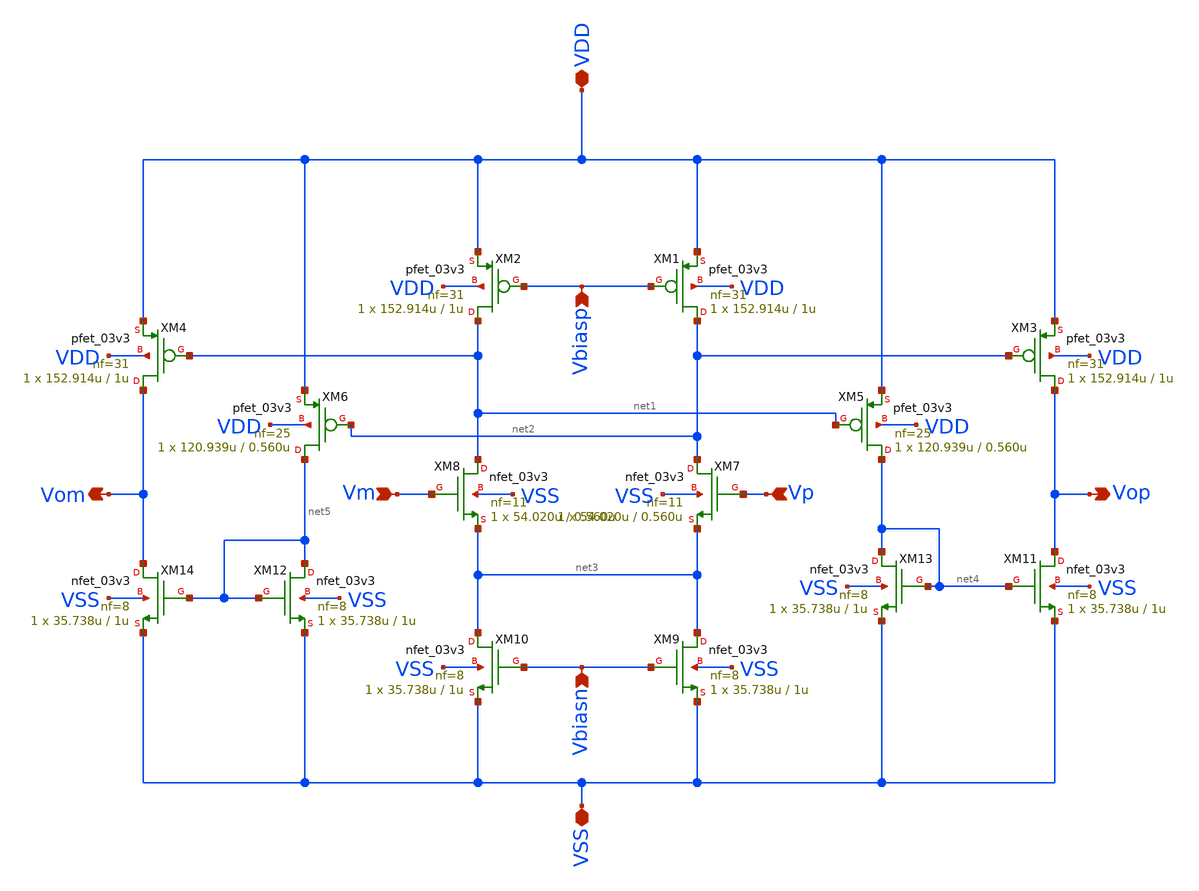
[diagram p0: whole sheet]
** sch_path: src/schematics/fullydiffamp/fullydiffamp.sch
**.subckt fullydiffamp VDD VSS Vbiasn Vbiasp Vm Vp Vom Vop
*.iopin VDD
*.iopin VSS
*.ipin Vbiasn
*.ipin Vbiasp
*.ipin Vm
*.ipin Vp
*.opin Vom
*.opin Vop
XM5 net4 net1 VDD VDD pfet_03v3 L=0.560u W=120.939u nf=25 ad='int((nf+1)/2) * W/nf * 0.18u' as='int((nf+2)/2) * W/nf * 0.18u'
+ pd='2*int((nf+1)/2) * (W/nf + 0.18u)' ps='2*int((nf+2)/2) * (W/nf + 0.18u)' nrd='0.18u / W' nrs='0.18u / W'
+ sa=0 sb=0 sd=0 m=1
XM2 net1 Vbiasp VDD VDD pfet_03v3 L=1u W=152.914u nf=31 ad='int((nf+1)/2) * W/nf * 0.18u' as='int((nf+2)/2) * W/nf * 0.18u'
+ pd='2*int((nf+1)/2) * (W/nf + 0.18u)' ps='2*int((nf+2)/2) * (W/nf + 0.18u)' nrd='0.18u / W' nrs='0.18u / W'
+ sa=0 sb=0 sd=0 m=1
XM8 net1 Vm net3 VSS nfet_03v3 L=0.560u W=54.020u nf=11 ad='int((nf+1)/2) * W/nf * 0.18u' as='int((nf+2)/2) * W/nf * 0.18u'
+ pd='2*int((nf+1)/2) * (W/nf + 0.18u)' ps='2*int((nf+2)/2) * (W/nf + 0.18u)' nrd='0.18u / W' nrs='0.18u / W'
+ sa=0 sb=0 sd=0 m=1
XM7 net2 Vp net3 VSS nfet_03v3 L=0.560u W=54.020u nf=11 ad='int((nf+1)/2) * W/nf * 0.18u' as='int((nf+2)/2) * W/nf * 0.18u'
+ pd='2*int((nf+1)/2) * (W/nf + 0.18u)' ps='2*int((nf+2)/2) * (W/nf + 0.18u)' nrd='0.18u / W' nrs='0.18u / W'
+ sa=0 sb=0 sd=0 m=1
XM1 net2 Vbiasp VDD VDD pfet_03v3 L=1u W=152.914u nf=31 ad='int((nf+1)/2) * W/nf * 0.18u' as='int((nf+2)/2) * W/nf * 0.18u'
+ pd='2*int((nf+1)/2) * (W/nf + 0.18u)' ps='2*int((nf+2)/2) * (W/nf + 0.18u)' nrd='0.18u / W' nrs='0.18u / W'
+ sa=0 sb=0 sd=0 m=1
XM6 net5 net2 VDD VDD pfet_03v3 L=0.560u W=120.939u nf=25 ad='int((nf+1)/2) * W/nf * 0.18u' as='int((nf+2)/2) * W/nf * 0.18u'
+ pd='2*int((nf+1)/2) * (W/nf + 0.18u)' ps='2*int((nf+2)/2) * (W/nf + 0.18u)' nrd='0.18u / W' nrs='0.18u / W'
+ sa=0 sb=0 sd=0 m=1
XM4 Vom net1 VDD VDD pfet_03v3 L=1u W=152.914u nf=31 ad='int((nf+1)/2) * W/nf * 0.18u' as='int((nf+2)/2) * W/nf * 0.18u'
+ pd='2*int((nf+1)/2) * (W/nf + 0.18u)' ps='2*int((nf+2)/2) * (W/nf + 0.18u)' nrd='0.18u / W' nrs='0.18u / W'
+ sa=0 sb=0 sd=0 m=1
XM3 Vop net2 VDD VDD pfet_03v3 L=1u W=152.914u nf=31 ad='int((nf+1)/2) * W/nf * 0.18u' as='int((nf+2)/2) * W/nf * 0.18u'
+ pd='2*int((nf+1)/2) * (W/nf + 0.18u)' ps='2*int((nf+2)/2) * (W/nf + 0.18u)' nrd='0.18u / W' nrs='0.18u / W'
+ sa=0 sb=0 sd=0 m=1
XM9 net3 Vbiasn VSS VSS nfet_03v3 L=1u W=35.738u nf=8 ad='int((nf+1)/2) * W/nf * 0.18u' as='int((nf+2)/2) * W/nf * 0.18u'
+ pd='2*int((nf+1)/2) * (W/nf + 0.18u)' ps='2*int((nf+2)/2) * (W/nf + 0.18u)' nrd='0.18u / W' nrs='0.18u / W'
+ sa=0 sb=0 sd=0 m=1
XM10 net3 Vbiasn VSS VSS nfet_03v3 L=1u W=35.738u nf=8 ad='int((nf+1)/2) * W/nf * 0.18u' as='int((nf+2)/2) * W/nf * 0.18u'
+ pd='2*int((nf+1)/2) * (W/nf + 0.18u)' ps='2*int((nf+2)/2) * (W/nf + 0.18u)' nrd='0.18u / W' nrs='0.18u / W'
+ sa=0 sb=0 sd=0 m=1
XM11 Vop net4 VSS VSS nfet_03v3 L=1u W=35.738u nf=8 ad='int((nf+1)/2) * W/nf * 0.18u' as='int((nf+2)/2) * W/nf * 0.18u'
+ pd='2*int((nf+1)/2) * (W/nf + 0.18u)' ps='2*int((nf+2)/2) * (W/nf + 0.18u)' nrd='0.18u / W' nrs='0.18u / W'
+ sa=0 sb=0 sd=0 m=1
XM13 net4 net4 VSS VSS nfet_03v3 L=1u W=35.738u nf=8 ad='int((nf+1)/2) * W/nf * 0.18u' as='int((nf+2)/2) * W/nf * 0.18u'
+ pd='2*int((nf+1)/2) * (W/nf + 0.18u)' ps='2*int((nf+2)/2) * (W/nf + 0.18u)' nrd='0.18u / W' nrs='0.18u / W'
+ sa=0 sb=0 sd=0 m=1
XM12 net5 net5 VSS VSS nfet_03v3 L=1u W=35.738u nf=8 ad='int((nf+1)/2) * W/nf * 0.18u' as='int((nf+2)/2) * W/nf * 0.18u'
+ pd='2*int((nf+1)/2) * (W/nf + 0.18u)' ps='2*int((nf+2)/2) * (W/nf + 0.18u)' nrd='0.18u / W' nrs='0.18u / W'
+ sa=0 sb=0 sd=0 m=1
XM14 Vom net5 VSS VSS nfet_03v3 L=1u W=35.738u nf=8 ad='int((nf+1)/2) * W/nf * 0.18u' as='int((nf+2)/2) * W/nf * 0.18u'
+ pd='2*int((nf+1)/2) * (W/nf + 0.18u)' ps='2*int((nf+2)/2) * (W/nf + 0.18u)' nrd='0.18u / W' nrs='0.18u / W'
+ sa=0 sb=0 sd=0 m=1
**.ends
.end
